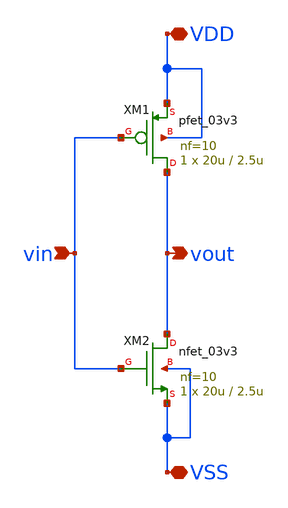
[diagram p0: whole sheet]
** sch_path: macros/inverter/schematic/xschem/inverter.sch
**.subckt inverter VDD VSS vin vout
*.iopin VDD
*.iopin VSS
*.ipin vin
*.opin vout
XM1 vout vin VDD VDD pfet_03v3 L=2.5u W=20u nf=10 ad='int((nf+1)/2) * W/nf * 0.18u' as='int((nf+2)/2) * W/nf * 0.18u'
+ pd='2*int((nf+1)/2) * (W/nf + 0.18u)' ps='2*int((nf+2)/2) * (W/nf + 0.18u)' nrd='0.18u / W' nrs='0.18u / W'
+ sa=0 sb=0 sd=0 m=1 par=1
XM2 vout vin VSS VSS nfet_03v3 L=2.5u W=20u nf=10 ad='int((nf+1)/2) * W/nf * 0.18u' as='int((nf+2)/2) * W/nf * 0.18u'
+ pd='2*int((nf+1)/2) * (W/nf + 0.18u)' ps='2*int((nf+2)/2) * (W/nf + 0.18u)' nrd='0.18u / W' nrs='0.18u / W'
+ sa=0 sb=0 sd=0 m=1 par=1
**.ends
.end
